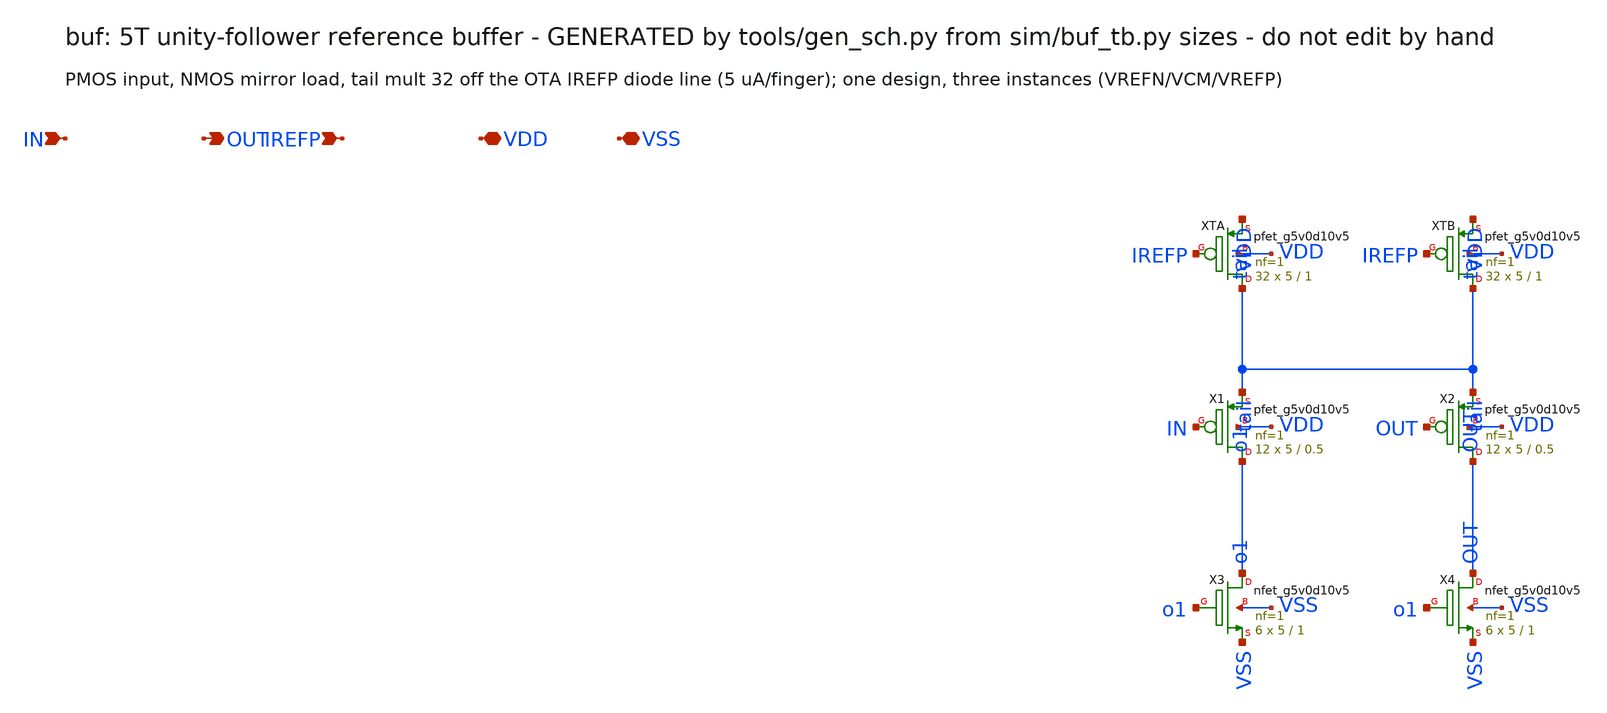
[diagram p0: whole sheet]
** sch_path: xschem/buf.sch
**.subckt buf IN OUT IREFP VDD VSS
*.ipin IN
*.opin OUT
*.ipin IREFP
*.iopin VDD
*.iopin VSS
XXTA tail IREFP VDD VDD sky130_fd_pr__pfet_g5v0d10v5 L=1 W=5 nf=1 ad=0 as=0 pd=0 ps=0 nrd=0 nrs=0
+ sa=0 sb=0 sd=0 mult=32 m=32
XXTB tail IREFP VDD VDD sky130_fd_pr__pfet_g5v0d10v5 L=1 W=5 nf=1 ad=0 as=0 pd=0 ps=0 nrd=0 nrs=0
+ sa=0 sb=0 sd=0 mult=32 m=32
XX1 o1 IN tail VDD sky130_fd_pr__pfet_g5v0d10v5 L=0.5 W=5 nf=1 ad=0 as=0 pd=0 ps=0 nrd=0 nrs=0 sa=0
+ sb=0 sd=0 mult=12 m=12
XX2 OUT OUT tail VDD sky130_fd_pr__pfet_g5v0d10v5 L=0.5 W=5 nf=1 ad=0 as=0 pd=0 ps=0 nrd=0 nrs=0
+ sa=0 sb=0 sd=0 mult=12 m=12
XX3 o1 o1 VSS VSS sky130_fd_pr__nfet_g5v0d10v5 L=1 W=5 nf=1 ad=0 as=0 pd=0 ps=0 nrd=0 nrs=0 sa=0
+ sb=0 sd=0 mult=6 m=6
XX4 OUT o1 VSS VSS sky130_fd_pr__nfet_g5v0d10v5 L=1 W=5 nf=1 ad=0 as=0 pd=0 ps=0 nrd=0 nrs=0 sa=0
+ sb=0 sd=0 mult=6 m=6
**.ends
.end
